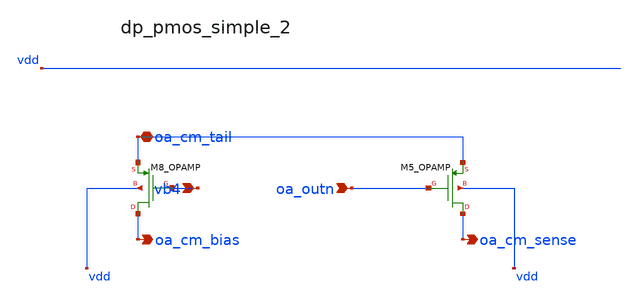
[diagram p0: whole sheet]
** sch_path: analog-db/raw/sup_003_rrl_sc_integrator/hier/blocks/dp_pmos_simple_2.sch
**.subckt dp_pmos_simple_2 vb4 oa_outn oa_cm_tail oa_cm_bias oa_cm_sense
*.ipin vb4
*.ipin oa_outn
*.iopin oa_cm_tail
*.opin oa_cm_bias
*.opin oa_cm_sense
XM5_OPAMP oa_cm_sense oa_outn oa_cm_tail vdd sg13_lv_pmos w=x_dut_xm5_opamp_w l=x_dut_xm5_opamp_l
+ ng=1 m=x_dut_xm5_opamp_m
XM8_OPAMP oa_cm_bias vb4 oa_cm_tail vdd sg13_lv_pmos w=x_dut_xm8_opamp_w l=x_dut_xm8_opamp_l ng=1
+ m=x_dut_xm8_opamp_m
**.ends
.end
